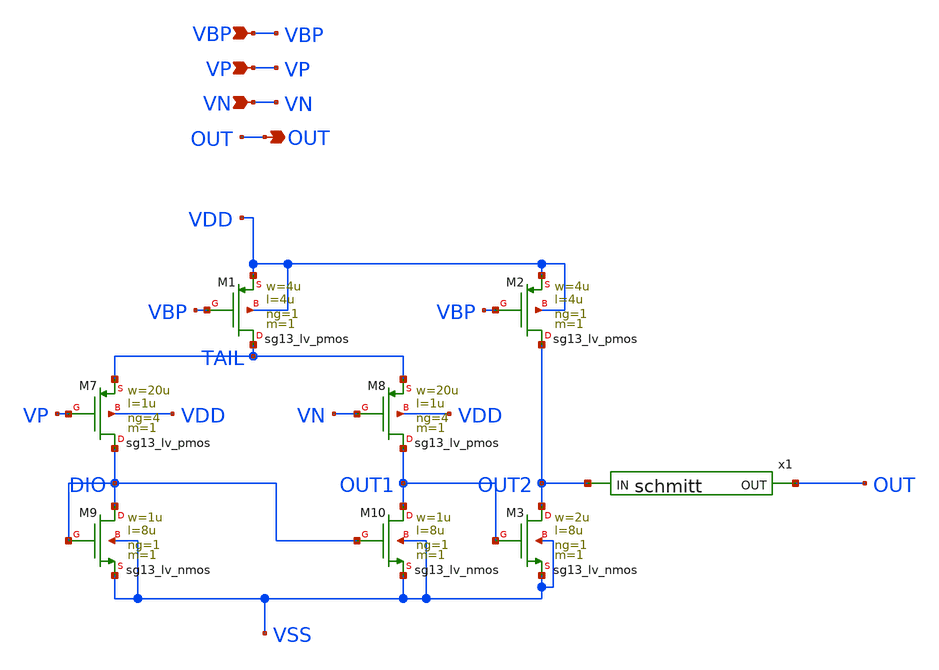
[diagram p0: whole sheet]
** sch_path: design/blocks/comparator/schematic/comp_inf.sch
**.subckt comp_inf OUT VN VP VBP
*.opin OUT
*.ipin VN
*.ipin VP
*.ipin VBP
XM1 TAIL VBP VDD VDD sg13_lv_pmos w=4u l=4u ng=1 m=1 mm_ok=1
XM7 DIO VP TAIL VDD sg13_lv_pmos w=20u l=1u ng=4 m=1 mm_ok=1
XM8 OUT1 VN TAIL VDD sg13_lv_pmos w=20u l=1u ng=4 m=1 mm_ok=1
XM9 DIO DIO VSS VSS sg13_lv_nmos w=1u l=8u ng=1 m=1 mm_ok=1
XM10 OUT1 DIO VSS VSS sg13_lv_nmos w=1u l=8u ng=1 m=1 mm_ok=1
XM2 OUT2 VBP VDD VDD sg13_lv_pmos w=4u l=4u ng=1 m=1 mm_ok=1
XM3 OUT2 OUT1 VSS VSS sg13_lv_nmos w=2u l=8u ng=1 m=1 mm_ok=1
x1 OUT2 OUT VDD VSS schmitt
**.ends

* expanding   symbol:  schmitt.sym # of pins=2
** sym_path: design/blocks/schmitt/schematic/schmitt.sym
** sch_path: design/blocks/schmitt/schematic/schmitt.sch
.subckt schmitt IN OUT VDD VSS
*.opin OUT
*.ipin IN
XM4 P_MID IN VDD VDD sg13_lv_pmos w=1.04u l=0.13u ng=1 m=1 mm_ok=1
XM6 OUT IN N_MID VSS sg13_lv_nmos w=0.76u l=0.13u ng=1 m=1 mm_ok=1
XM5 OUT IN P_MID VDD sg13_lv_pmos w=1.04u l=0.13u ng=1 m=1 mm_ok=1
XM7 N_MID IN VSS VSS sg13_lv_nmos w=0.76u l=0.13u ng=1 m=1 mm_ok=1
XM8 VSS OUT P_MID VDD sg13_lv_pmos w=0.42u l=0.13u ng=1 m=1 mm_ok=1
XM9 VDD OUT N_MID VSS sg13_lv_nmos w=0.42u l=0.13u ng=1 m=1 mm_ok=1
.ends

.end
